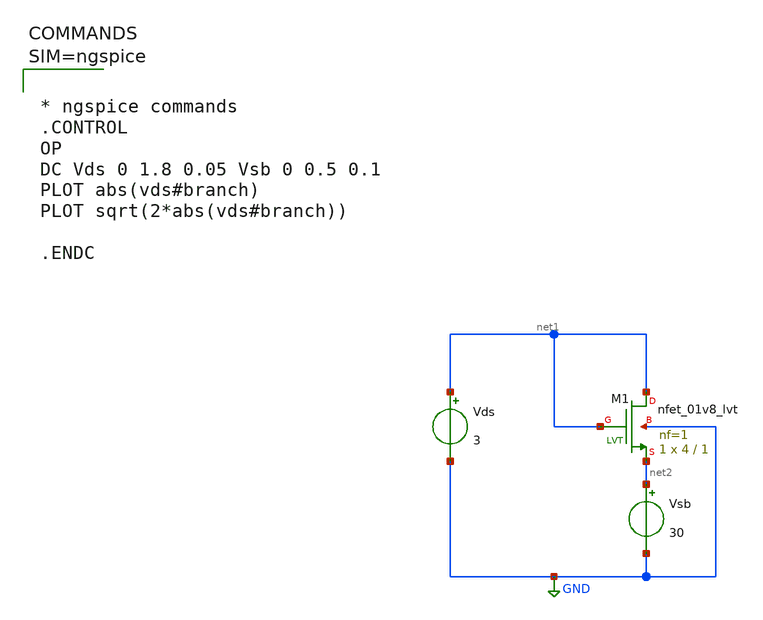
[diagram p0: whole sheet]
** sch_path: xschem/untitled-5.sch
**.subckt untitled-5
XM1 net1 net1 net2 GND sky130_fd_pr__nfet_01v8_lvt L=1 W=4 nf=1 ad='int((1 + 1)/2) * 4 / 1 * 0.29' as='int((1 + 2)/2) * 4 / 1 * 0.29'
+ pd='2*int((1 + 1)/2) * (4 / 1 + 0.29)' ps='2*int((1 + 2)/2) * (4 / 1 + 0.29)' nrd='0.29 / 4 ' nrs='0.29 / 4 '
+ sa=0 sb=0 sd=0 mult=1 m=1
Vds net1 GND 3
Vsb net2 GND 30
**** begin user architecture code



* ngspice commands
.CONTROL
OP
DC Vds 0 1.8 0.05 Vsb 0 0.5 0.1
PLOT abs(vds#branch)
PLOT sqrt(2*abs(vds#branch))

.ENDC




** opencircuitdesign pdks install
.lib $::SKYWATER_MODELS/sky130.lib.spice tt

**** end user architecture code
**.ends
.GLOBAL GND
.end
